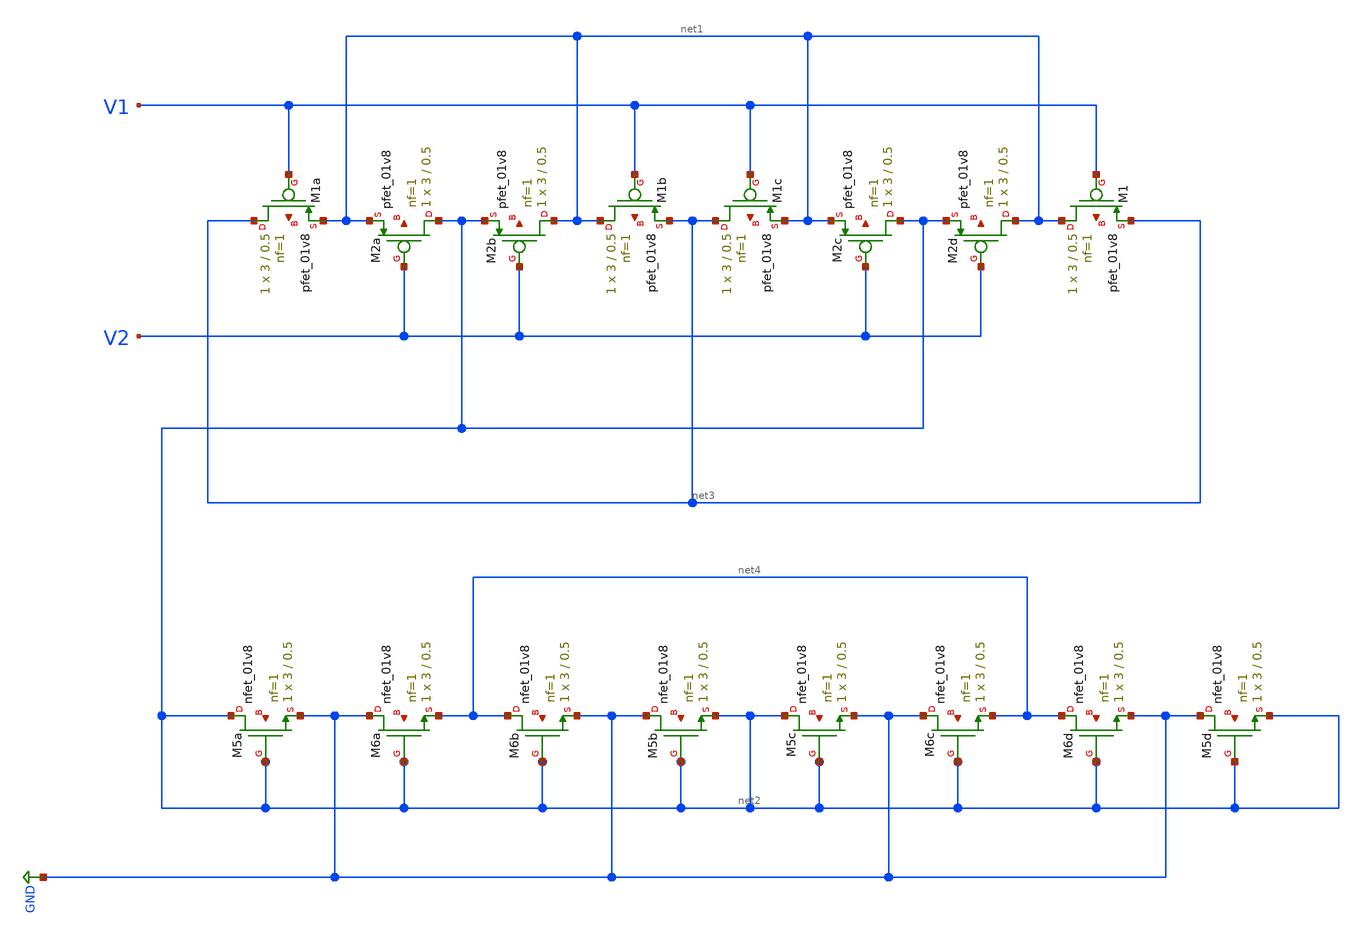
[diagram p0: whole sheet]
** sch_path: xsch/ip/test/cmdiffamp.sch
**.subckt cmdiffamp
XM1a net3 V1 net1 net5 sky130_fd_pr__pfet_01v8 L=0.5 W=3 nf=1 ad='int((nf+1)/2) * W/nf * 0.29' as='int((nf+2)/2) * W/nf * 0.29'
+ pd='2*int((nf+1)/2) * (W/nf + 0.29)' ps='2*int((nf+2)/2) * (W/nf + 0.29)' nrd='0.29 / W' nrs='0.29 / W'
+ sa=0 sb=0 sd=0 mult=1 m=1
XM1b net1 V1 net3 net6 sky130_fd_pr__pfet_01v8 L=0.5 W=3 nf=1 ad='int((nf+1)/2) * W/nf * 0.29' as='int((nf+2)/2) * W/nf * 0.29'
+ pd='2*int((nf+1)/2) * (W/nf + 0.29)' ps='2*int((nf+2)/2) * (W/nf + 0.29)' nrd='0.29 / W' nrs='0.29 / W'
+ sa=0 sb=0 sd=0 mult=1 m=1
XM1c net3 V1 net1 net7 sky130_fd_pr__pfet_01v8 L=0.5 W=3 nf=1 ad='int((nf+1)/2) * W/nf * 0.29' as='int((nf+2)/2) * W/nf * 0.29'
+ pd='2*int((nf+1)/2) * (W/nf + 0.29)' ps='2*int((nf+2)/2) * (W/nf + 0.29)' nrd='0.29 / W' nrs='0.29 / W'
+ sa=0 sb=0 sd=0 mult=1 m=1
XM2a net2 V2 net1 net8 sky130_fd_pr__pfet_01v8 L=0.5 W=3 nf=1 ad='int((nf+1)/2) * W/nf * 0.29' as='int((nf+2)/2) * W/nf * 0.29'
+ pd='2*int((nf+1)/2) * (W/nf + 0.29)' ps='2*int((nf+2)/2) * (W/nf + 0.29)' nrd='0.29 / W' nrs='0.29 / W'
+ sa=0 sb=0 sd=0 mult=1 m=1
XM2b net1 V2 net2 net9 sky130_fd_pr__pfet_01v8 L=0.5 W=3 nf=1 ad='int((nf+1)/2) * W/nf * 0.29' as='int((nf+2)/2) * W/nf * 0.29'
+ pd='2*int((nf+1)/2) * (W/nf + 0.29)' ps='2*int((nf+2)/2) * (W/nf + 0.29)' nrd='0.29 / W' nrs='0.29 / W'
+ sa=0 sb=0 sd=0 mult=1 m=1
XM2c net2 V2 net1 net10 sky130_fd_pr__pfet_01v8 L=0.5 W=3 nf=1 ad='int((nf+1)/2) * W/nf * 0.29' as='int((nf+2)/2) * W/nf * 0.29'
+ pd='2*int((nf+1)/2) * (W/nf + 0.29)' ps='2*int((nf+2)/2) * (W/nf + 0.29)' nrd='0.29 / W' nrs='0.29 / W'
+ sa=0 sb=0 sd=0 mult=1 m=1
XM2d net1 V2 net2 net11 sky130_fd_pr__pfet_01v8 L=0.5 W=3 nf=1 ad='int((nf+1)/2) * W/nf * 0.29' as='int((nf+2)/2) * W/nf * 0.29'
+ pd='2*int((nf+1)/2) * (W/nf + 0.29)' ps='2*int((nf+2)/2) * (W/nf + 0.29)' nrd='0.29 / W' nrs='0.29 / W'
+ sa=0 sb=0 sd=0 mult=1 m=1
XM1 net1 V1 net3 net12 sky130_fd_pr__pfet_01v8 L=0.5 W=3 nf=1 ad='int((nf+1)/2) * W/nf * 0.29' as='int((nf+2)/2) * W/nf * 0.29'
+ pd='2*int((nf+1)/2) * (W/nf + 0.29)' ps='2*int((nf+2)/2) * (W/nf + 0.29)' nrd='0.29 / W' nrs='0.29 / W'
+ sa=0 sb=0 sd=0 mult=1 m=1
XM5a net2 net2 GND net13 sky130_fd_pr__nfet_01v8 L=0.5 W=3 nf=1 ad='int((nf+1)/2) * W/nf * 0.29' as='int((nf+2)/2) * W/nf * 0.29'
+ pd='2*int((nf+1)/2) * (W/nf + 0.29)' ps='2*int((nf+2)/2) * (W/nf + 0.29)' nrd='0.29 / W' nrs='0.29 / W'
+ sa=0 sb=0 sd=0 mult=1 m=1
XM6a GND net2 net4 net14 sky130_fd_pr__nfet_01v8 L=0.5 W=3 nf=1 ad='int((nf+1)/2) * W/nf * 0.29' as='int((nf+2)/2) * W/nf * 0.29'
+ pd='2*int((nf+1)/2) * (W/nf + 0.29)' ps='2*int((nf+2)/2) * (W/nf + 0.29)' nrd='0.29 / W' nrs='0.29 / W'
+ sa=0 sb=0 sd=0 mult=1 m=1
XM6b net4 net2 GND net15 sky130_fd_pr__nfet_01v8 L=0.5 W=3 nf=1 ad='int((nf+1)/2) * W/nf * 0.29' as='int((nf+2)/2) * W/nf * 0.29'
+ pd='2*int((nf+1)/2) * (W/nf + 0.29)' ps='2*int((nf+2)/2) * (W/nf + 0.29)' nrd='0.29 / W' nrs='0.29 / W'
+ sa=0 sb=0 sd=0 mult=1 m=1
XM5b GND net2 net2 net16 sky130_fd_pr__nfet_01v8 L=0.5 W=3 nf=1 ad='int((nf+1)/2) * W/nf * 0.29' as='int((nf+2)/2) * W/nf * 0.29'
+ pd='2*int((nf+1)/2) * (W/nf + 0.29)' ps='2*int((nf+2)/2) * (W/nf + 0.29)' nrd='0.29 / W' nrs='0.29 / W'
+ sa=0 sb=0 sd=0 mult=1 m=1
XM5c net2 net2 GND net17 sky130_fd_pr__nfet_01v8 L=0.5 W=3 nf=1 ad='int((nf+1)/2) * W/nf * 0.29' as='int((nf+2)/2) * W/nf * 0.29'
+ pd='2*int((nf+1)/2) * (W/nf + 0.29)' ps='2*int((nf+2)/2) * (W/nf + 0.29)' nrd='0.29 / W' nrs='0.29 / W'
+ sa=0 sb=0 sd=0 mult=1 m=1
XM6c GND net2 net4 net18 sky130_fd_pr__nfet_01v8 L=0.5 W=3 nf=1 ad='int((nf+1)/2) * W/nf * 0.29' as='int((nf+2)/2) * W/nf * 0.29'
+ pd='2*int((nf+1)/2) * (W/nf + 0.29)' ps='2*int((nf+2)/2) * (W/nf + 0.29)' nrd='0.29 / W' nrs='0.29 / W'
+ sa=0 sb=0 sd=0 mult=1 m=1
XM6d net4 net2 GND net19 sky130_fd_pr__nfet_01v8 L=0.5 W=3 nf=1 ad='int((nf+1)/2) * W/nf * 0.29' as='int((nf+2)/2) * W/nf * 0.29'
+ pd='2*int((nf+1)/2) * (W/nf + 0.29)' ps='2*int((nf+2)/2) * (W/nf + 0.29)' nrd='0.29 / W' nrs='0.29 / W'
+ sa=0 sb=0 sd=0 mult=1 m=1
XM5d GND net2 net2 net20 sky130_fd_pr__nfet_01v8 L=0.5 W=3 nf=1 ad='int((nf+1)/2) * W/nf * 0.29' as='int((nf+2)/2) * W/nf * 0.29'
+ pd='2*int((nf+1)/2) * (W/nf + 0.29)' ps='2*int((nf+2)/2) * (W/nf + 0.29)' nrd='0.29 / W' nrs='0.29 / W'
+ sa=0 sb=0 sd=0 mult=1 m=1
**.ends
.GLOBAL GND
.end
